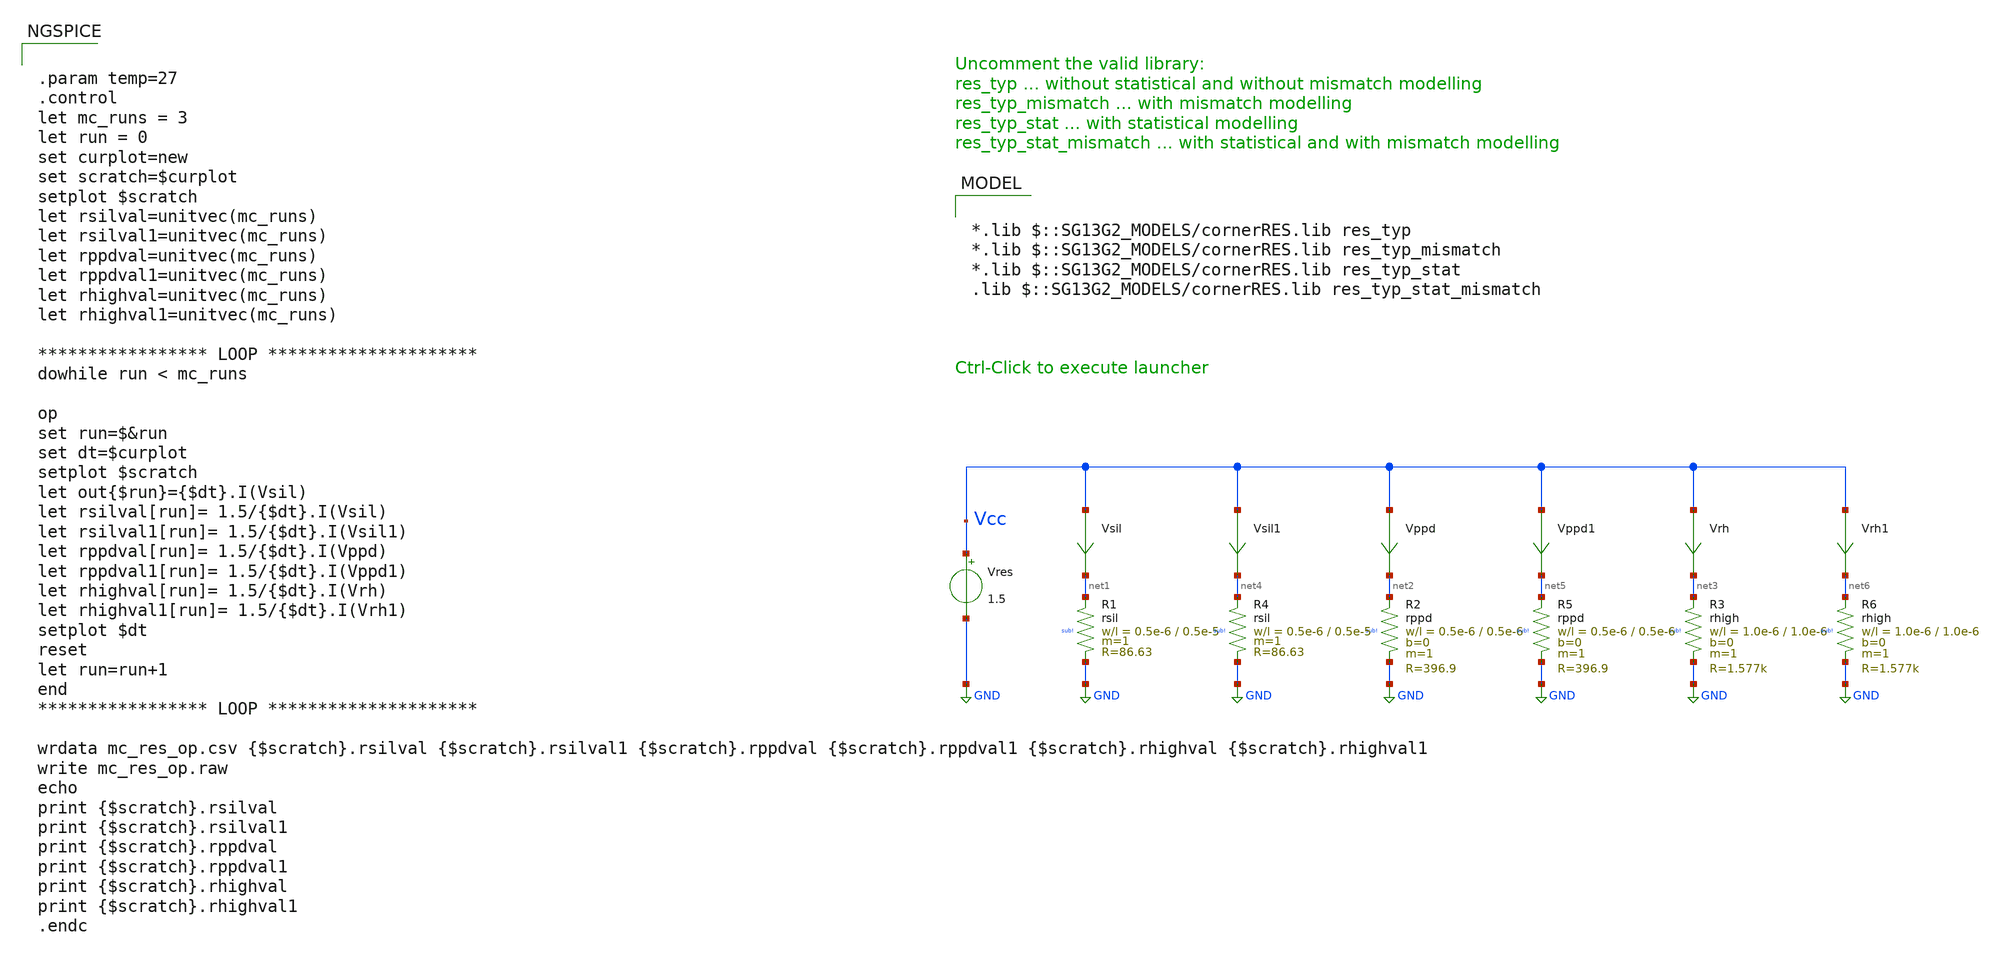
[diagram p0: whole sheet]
** sch_path: ihp-sg13g2/libs.tech/xschem/sg13g2_tests/mc_res_op.sch
* Copyright 2023 IHP PDK Authors
**.subckt mc_res_op
Vres Vcc GND 1.5
Vsil Vcc net1 0
.save i(vsil)
Vppd Vcc net2 0
.save i(vppd)
XR3 net3 GND sub! rhigh w=1.0e-6 l=1.0e-6 m=1 b=0 mm_ok=1
Vrh Vcc net3 0
.save i(vrh)
XR1 net1 GND sub! rsil w=0.5e-6 l=0.5e-5 m=1 mm_ok=1
XR2 net2 GND sub! rppd w=0.5e-6 l=0.5e-6 m=1 b=0 mm_ok=1
Vsil1 Vcc net4 0
.save i(vsil1)
XR4 net4 GND sub! rsil w=0.5e-6 l=0.5e-5 m=1 mm_ok=1
Vppd1 Vcc net5 0
.save i(vppd1)
XR5 net5 GND sub! rppd w=0.5e-6 l=0.5e-6 m=1 b=0 mm_ok=1
XR6 net6 GND sub! rhigh w=1.0e-6 l=1.0e-6 m=1 b=0 mm_ok=1
Vrh1 Vcc net6 0
.save i(vrh1)
**** begin user architecture code

*.lib $::SG13G2_MODELS/cornerRES.lib res_typ
*.lib $::SG13G2_MODELS/cornerRES.lib res_typ_mismatch
*.lib $::SG13G2_MODELS/cornerRES.lib res_typ_stat
.lib $::SG13G2_MODELS/cornerRES.lib res_typ_stat_mismatch



.param temp=27
.control
let mc_runs = 3
let run = 0
set curplot=new
set scratch=$curplot
setplot $scratch
let rsilval=unitvec(mc_runs)
let rsilval1=unitvec(mc_runs)
let rppdval=unitvec(mc_runs)
let rppdval1=unitvec(mc_runs)
let rhighval=unitvec(mc_runs)
let rhighval1=unitvec(mc_runs)

***************** LOOP *********************
dowhile run < mc_runs

op
set run=$&run
set dt=$curplot
setplot $scratch
let out{$run}={$dt}.I(Vsil)
let rsilval[run]= 1.5/{$dt}.I(Vsil)
let rsilval1[run]= 1.5/{$dt}.I(Vsil1)
let rppdval[run]= 1.5/{$dt}.I(Vppd)
let rppdval1[run]= 1.5/{$dt}.I(Vppd1)
let rhighval[run]= 1.5/{$dt}.I(Vrh)
let rhighval1[run]= 1.5/{$dt}.I(Vrh1)
setplot $dt
reset
let run=run+1
end
***************** LOOP *********************

wrdata mc_res_op.csv {$scratch}.rsilval {$scratch}.rsilval1 {$scratch}.rppdval {$scratch}.rppdval1 {$scratch}.rhighval
+ {$scratch}.rhighval1
write mc_res_op.raw
echo
print {$scratch}.rsilval
print {$scratch}.rsilval1
print {$scratch}.rppdval
print {$scratch}.rppdval1
print {$scratch}.rhighval
print {$scratch}.rhighval1
.endc


**** end user architecture code
**.ends
.GLOBAL GND
.end
